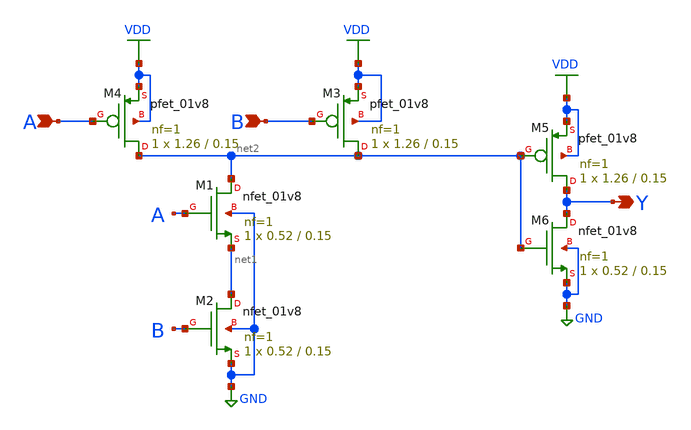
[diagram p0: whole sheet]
** sch_path: xschem/and21.sch
**.subckt and21 B A Y
*.ipin B
*.ipin A
*.opin Y
XM1 net2 A net1 GND sky130_fd_pr__nfet_01v8 L=0.15 W=0.52 nf=1 ad='int((nf+1)/2) * W/nf * 0.29' as='int((nf+2)/2) * W/nf * 0.29'
+ pd='2*int((nf+1)/2) * (W/nf + 0.29)' ps='2*int((nf+2)/2) * (W/nf + 0.29)' nrd='0.29 / W' nrs='0.29 / W'
+ sa=0 sb=0 sd=0 mult=1 m=1
XM2 net1 B GND GND sky130_fd_pr__nfet_01v8 L=0.15 W=0.52 nf=1 ad='int((nf+1)/2) * W/nf * 0.29' as='int((nf+2)/2) * W/nf * 0.29'
+ pd='2*int((nf+1)/2) * (W/nf + 0.29)' ps='2*int((nf+2)/2) * (W/nf + 0.29)' nrd='0.29 / W' nrs='0.29 / W'
+ sa=0 sb=0 sd=0 mult=1 m=1
XM3 net2 B VDD VDD sky130_fd_pr__pfet_01v8 L=0.15 W=1.26 nf=1 ad='int((nf+1)/2) * W/nf * 0.29' as='int((nf+2)/2) * W/nf * 0.29'
+ pd='2*int((nf+1)/2) * (W/nf + 0.29)' ps='2*int((nf+2)/2) * (W/nf + 0.29)' nrd='0.29 / W' nrs='0.29 / W'
+ sa=0 sb=0 sd=0 mult=1 m=1
XM4 net2 A VDD VDD sky130_fd_pr__pfet_01v8 L=0.15 W=1.26 nf=1 ad='int((nf+1)/2) * W/nf * 0.29' as='int((nf+2)/2) * W/nf * 0.29'
+ pd='2*int((nf+1)/2) * (W/nf + 0.29)' ps='2*int((nf+2)/2) * (W/nf + 0.29)' nrd='0.29 / W' nrs='0.29 / W'
+ sa=0 sb=0 sd=0 mult=1 m=1
XM5 Y net2 VDD VDD sky130_fd_pr__pfet_01v8 L=0.15 W=1.26 nf=1 ad='int((nf+1)/2) * W/nf * 0.29' as='int((nf+2)/2) * W/nf * 0.29'
+ pd='2*int((nf+1)/2) * (W/nf + 0.29)' ps='2*int((nf+2)/2) * (W/nf + 0.29)' nrd='0.29 / W' nrs='0.29 / W'
+ sa=0 sb=0 sd=0 mult=1 m=1
XM6 Y net2 GND GND sky130_fd_pr__nfet_01v8 L=0.15 W=0.52 nf=1 ad='int((nf+1)/2) * W/nf * 0.29' as='int((nf+2)/2) * W/nf * 0.29'
+ pd='2*int((nf+1)/2) * (W/nf + 0.29)' ps='2*int((nf+2)/2) * (W/nf + 0.29)' nrd='0.29 / W' nrs='0.29 / W'
+ sa=0 sb=0 sd=0 mult=1 m=1
**.ends
.GLOBAL GND
.GLOBAL VDD
.end
